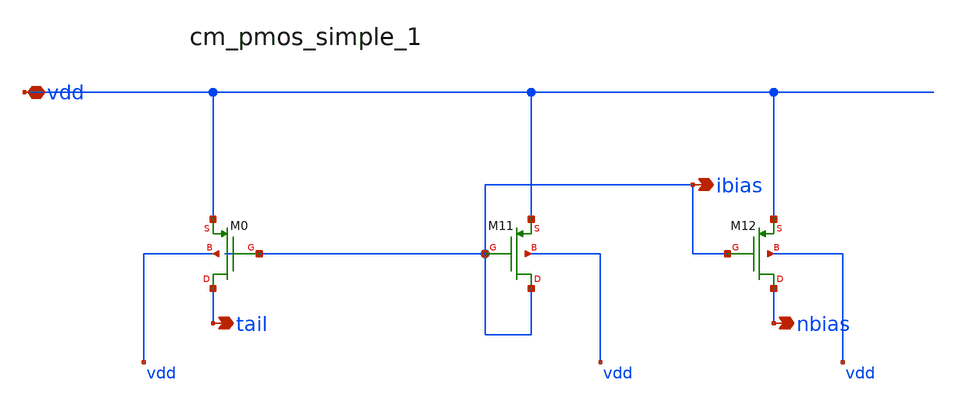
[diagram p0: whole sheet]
** sch_path: analog-db/raw/amp_004_folded_cascode/hier/blocks/cm_pmos_simple_1.sch
**.subckt cm_pmos_simple_1 vdd ibias tail nbias
*.iopin vdd
*.opin ibias
*.opin tail
*.opin nbias
XM0 tail ibias vdd vdd sg13_lv_pmos w=x_dut_xm0_w l=x_dut_xm0_l ng=x_dut_xm0_ng m=x_dut_xm0_m
XM11 ibias ibias vdd vdd sg13_lv_pmos w=x_dut_xm11_w l=x_dut_xm11_l ng=x_dut_xm11_ng m=x_dut_xm11_m
XM12 nbias ibias vdd vdd sg13_lv_pmos w=x_dut_xm12_w l=x_dut_xm12_l ng=x_dut_xm12_ng m=x_dut_xm12_m
**.ends
.end
